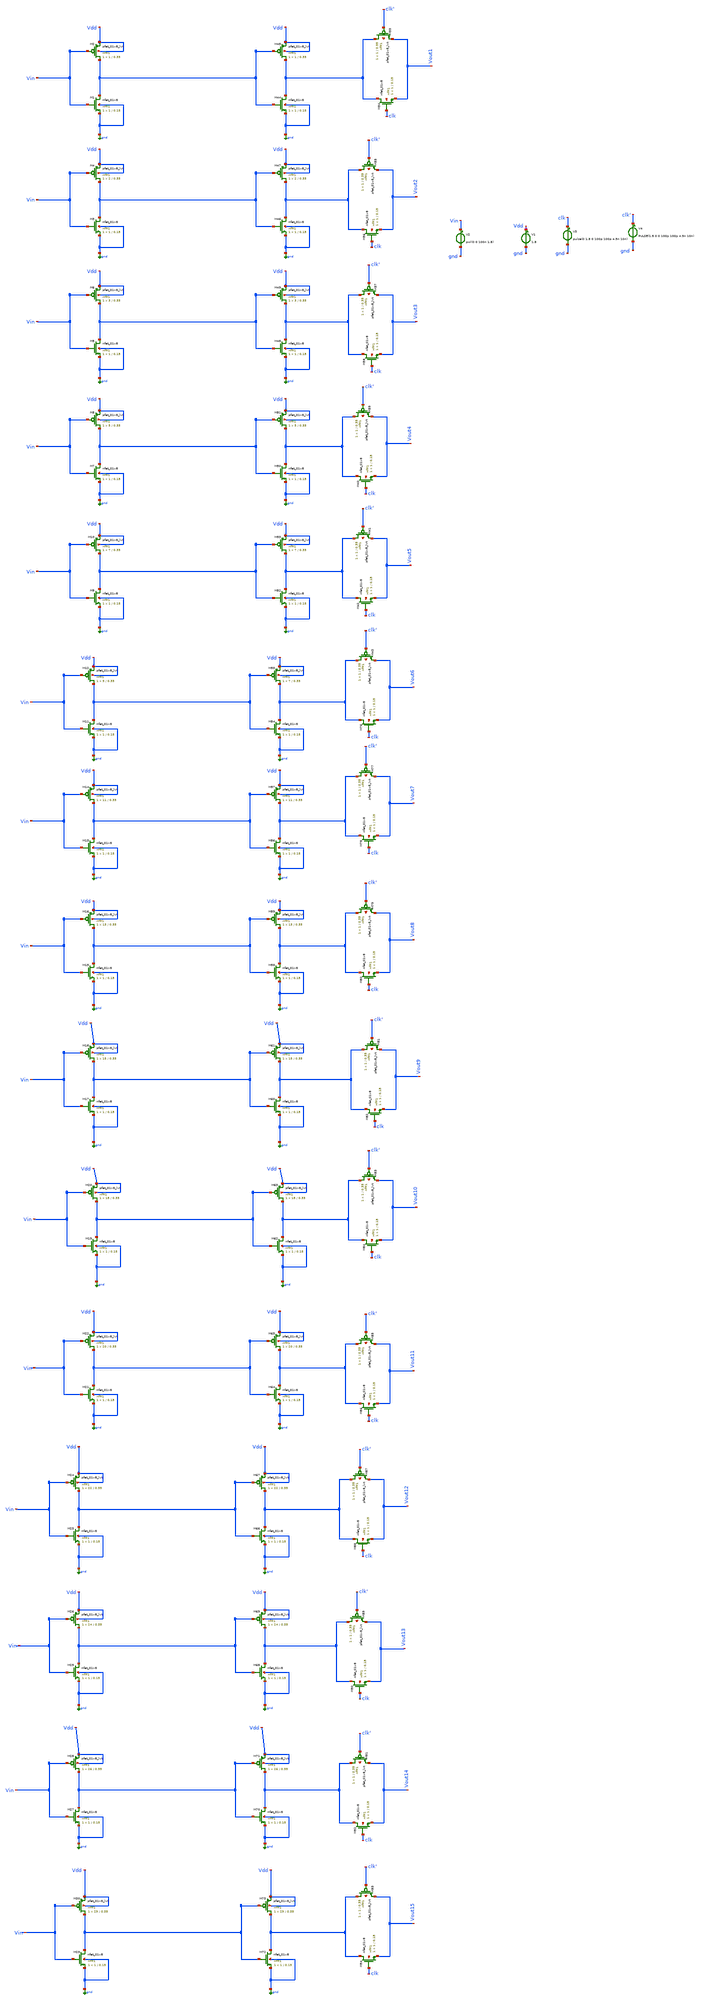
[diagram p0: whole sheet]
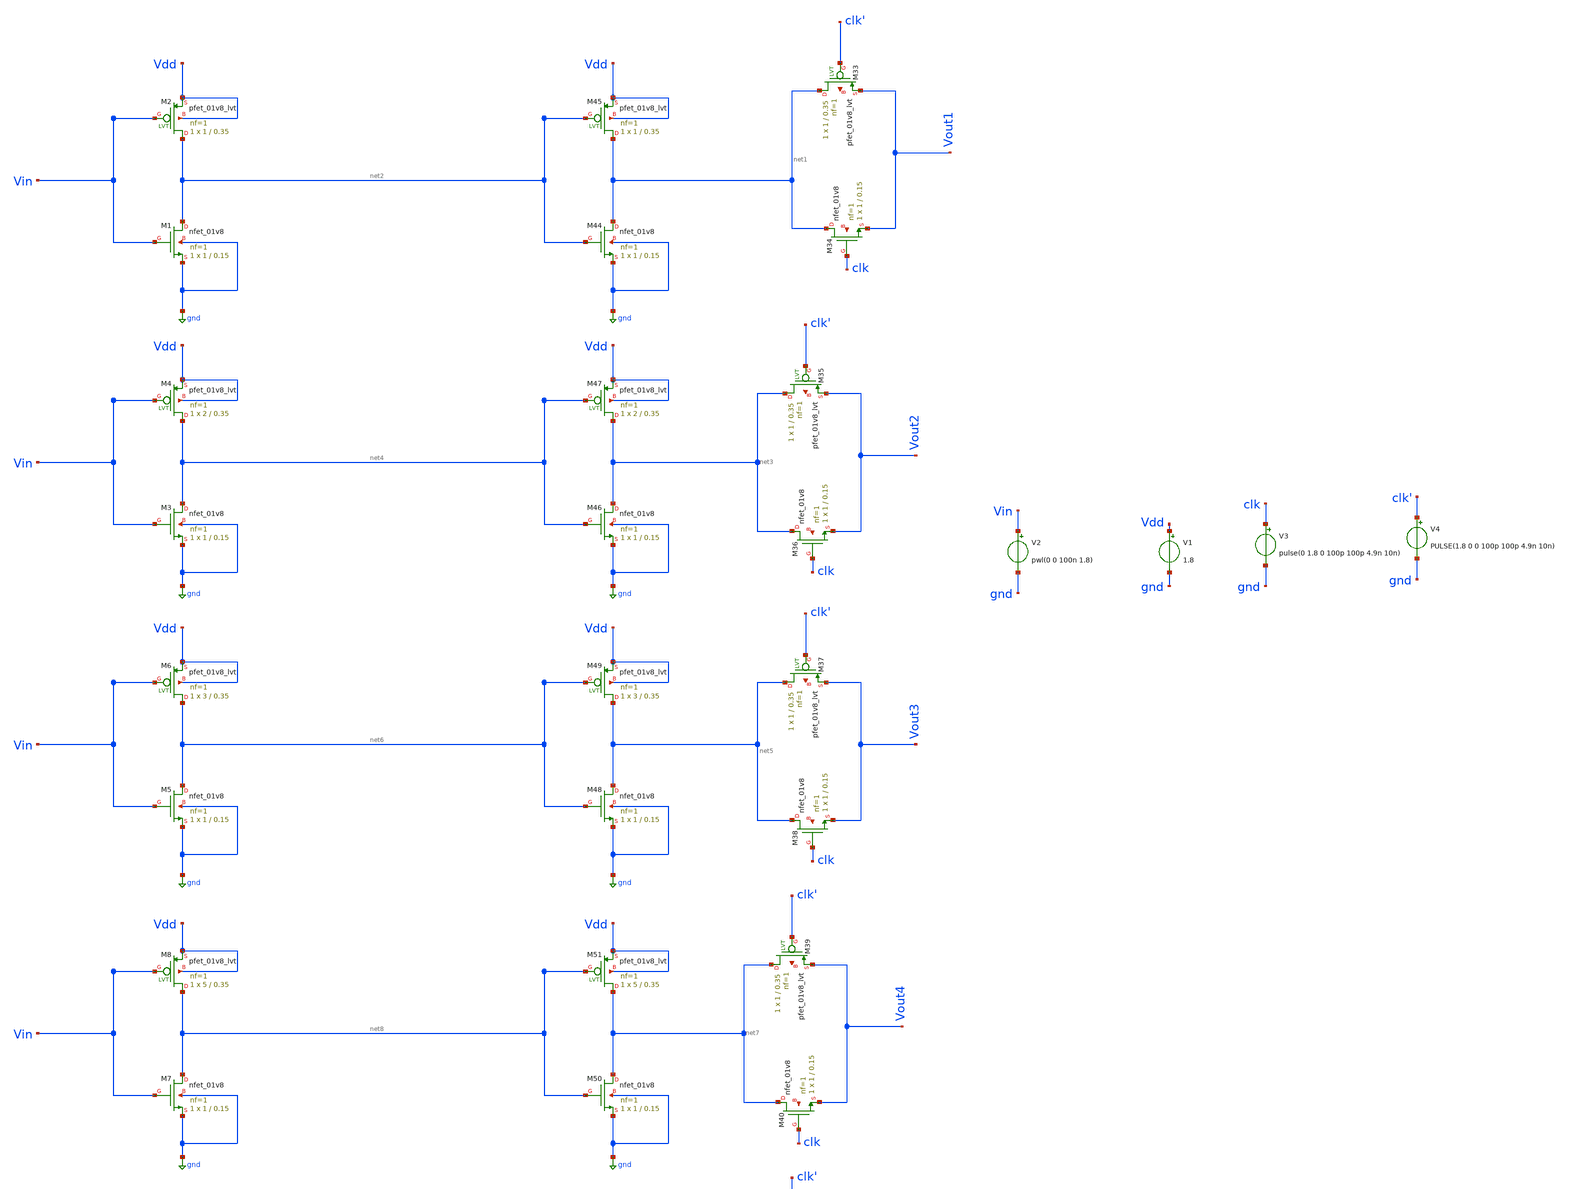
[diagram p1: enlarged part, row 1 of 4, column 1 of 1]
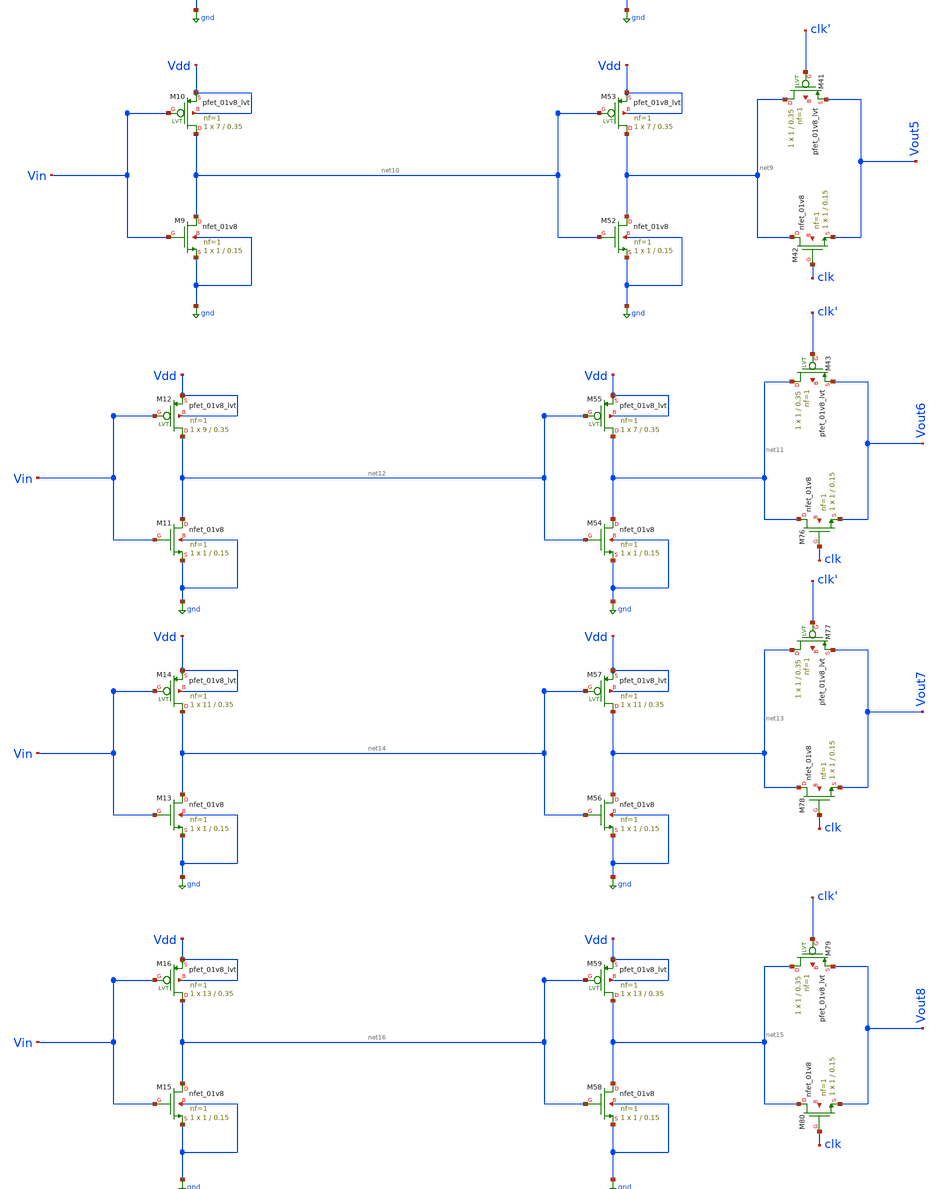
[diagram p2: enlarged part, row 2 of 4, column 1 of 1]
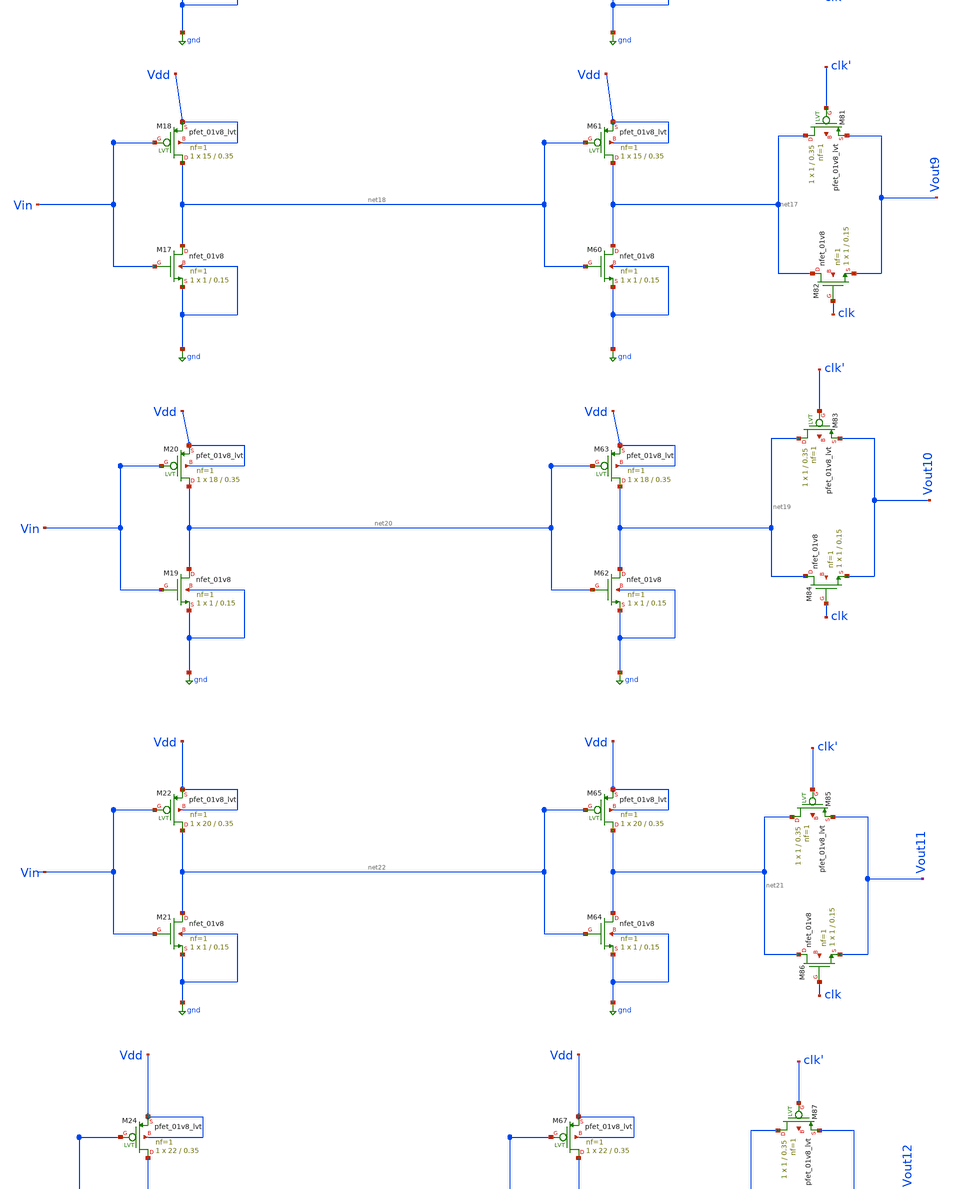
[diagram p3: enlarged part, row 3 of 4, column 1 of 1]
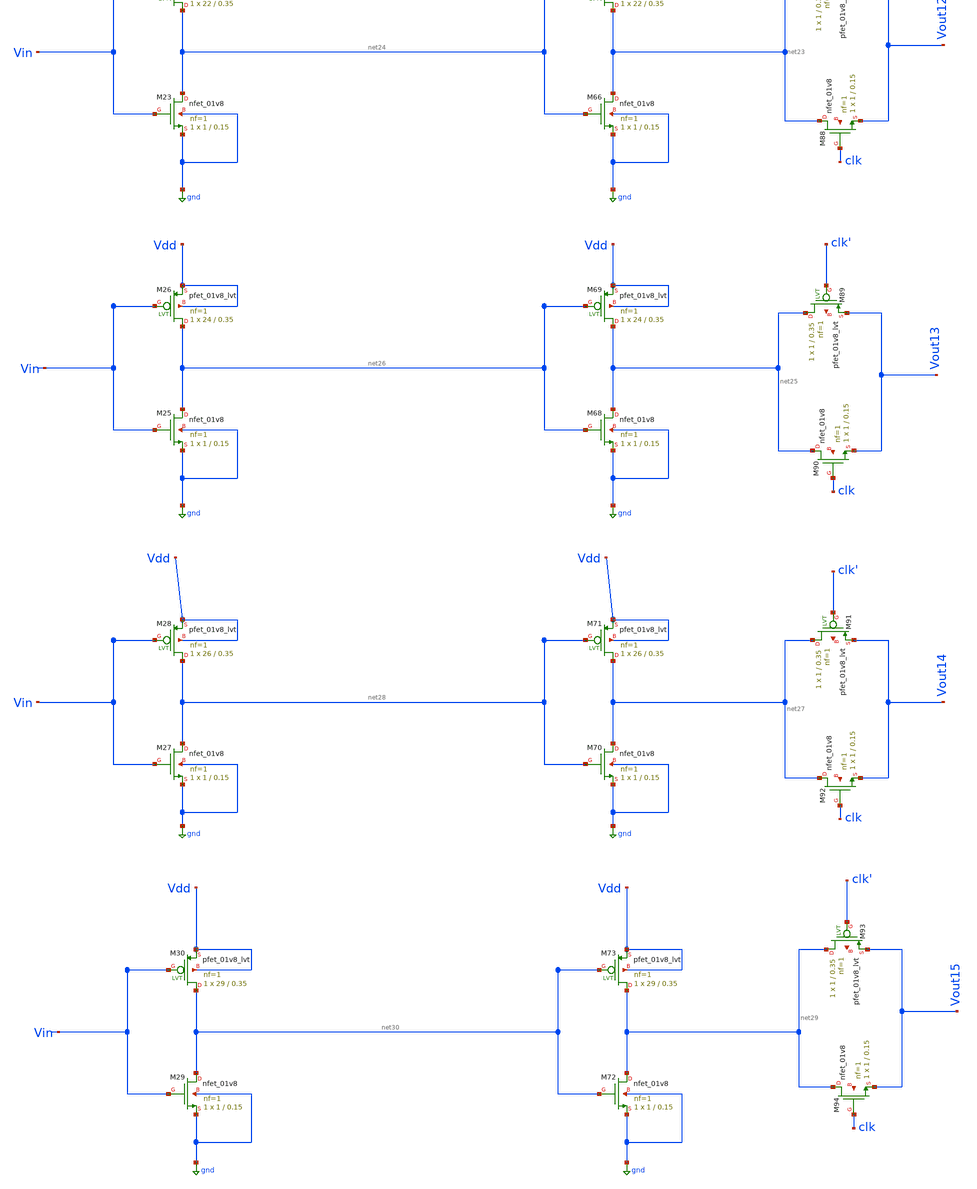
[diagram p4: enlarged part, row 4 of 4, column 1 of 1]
** sch_path: 4bit-tiq.sch
**.subckt 4bit-tiq
XM44 net1 net2 gnd gnd sky130_fd_pr__nfet_01v8 L=0.15 W=1 nf=1 ad='int((1 + 1)/2) * 1 / 1 * 0.29' as='int((1 + 2)/2) * 1 / 1 * 0.29'
+ pd='2*int((1 + 1)/2) * (1 / 1 + 0.29)' ps='2*int((1 + 2)/2) * (1 / 1 + 0.29)' nrd='0.29 / 1 ' nrs='0.29 / 1 '
+ sa=0 sb=0 sd=0 mult=1 m=1
XM45 net1 net2 Vdd Vdd sky130_fd_pr__pfet_01v8_lvt L=0.35 W=1 nf=1 ad='int((1 + 1)/2) * 1 / 1 * 0.29'
+ as='int((1 + 2)/2) * 1 / 1 * 0.29' pd='2*int((1 + 1)/2) * (1 / 1 + 0.29)' ps='2*int((1 + 2)/2) * (1 / 1 + 0.29)'
+ nrd='0.29 / 1 ' nrs='0.29 / 1 ' sa=0 sb=0 sd=0 mult=1 m=1
V1 Vdd gnd 1.8
V2 Vin gnd pwl(0 0 100n 1.8)
XM46 net3 net4 gnd gnd sky130_fd_pr__nfet_01v8 L=0.15 W=1 nf=1 ad='int((1 + 1)/2) * 1 / 1 * 0.29' as='int((1 + 2)/2) * 1 / 1 * 0.29'
+ pd='2*int((1 + 1)/2) * (1 / 1 + 0.29)' ps='2*int((1 + 2)/2) * (1 / 1 + 0.29)' nrd='0.29 / 1 ' nrs='0.29 / 1 '
+ sa=0 sb=0 sd=0 mult=1 m=1
XM47 net3 net4 Vdd Vdd sky130_fd_pr__pfet_01v8_lvt L=0.35 W=2 nf=1 ad='int((1 + 1)/2) * 2 / 1 * 0.29'
+ as='int((1 + 2)/2) * 2 / 1 * 0.29' pd='2*int((1 + 1)/2) * (2 / 1 + 0.29)' ps='2*int((1 + 2)/2) * (2 / 1 + 0.29)'
+ nrd='0.29 / 2 ' nrs='0.29 / 2 ' sa=0 sb=0 sd=0 mult=1 m=1
XM48 net5 net6 gnd gnd sky130_fd_pr__nfet_01v8 L=0.15 W=1 nf=1 ad='int((1 + 1)/2) * 1 / 1 * 0.29' as='int((1 + 2)/2) * 1 / 1 * 0.29'
+ pd='2*int((1 + 1)/2) * (1 / 1 + 0.29)' ps='2*int((1 + 2)/2) * (1 / 1 + 0.29)' nrd='0.29 / 1 ' nrs='0.29 / 1 '
+ sa=0 sb=0 sd=0 mult=1 m=1
XM49 net5 net6 Vdd Vdd sky130_fd_pr__pfet_01v8_lvt L=0.35 W=3 nf=1 ad='int((1 + 1)/2) * 3 / 1 * 0.29'
+ as='int((1 + 2)/2) * 3 / 1 * 0.29' pd='2*int((1 + 1)/2) * (3 / 1 + 0.29)' ps='2*int((1 + 2)/2) * (3 / 1 + 0.29)'
+ nrd='0.29 / 3 ' nrs='0.29 / 3 ' sa=0 sb=0 sd=0 mult=1 m=1
XM50 net7 net8 gnd gnd sky130_fd_pr__nfet_01v8 L=0.15 W=1 nf=1 ad='int((1 + 1)/2) * 1 / 1 * 0.29' as='int((1 + 2)/2) * 1 / 1 * 0.29'
+ pd='2*int((1 + 1)/2) * (1 / 1 + 0.29)' ps='2*int((1 + 2)/2) * (1 / 1 + 0.29)' nrd='0.29 / 1 ' nrs='0.29 / 1 '
+ sa=0 sb=0 sd=0 mult=1 m=1
XM51 net7 net8 Vdd Vdd sky130_fd_pr__pfet_01v8_lvt L=0.35 W=5 nf=1 ad='int((1 + 1)/2) * 5 / 1 * 0.29'
+ as='int((1 + 2)/2) * 5 / 1 * 0.29' pd='2*int((1 + 1)/2) * (5 / 1 + 0.29)' ps='2*int((1 + 2)/2) * (5 / 1 + 0.29)'
+ nrd='0.29 / 5 ' nrs='0.29 / 5 ' sa=0 sb=0 sd=0 mult=1 m=1
XM52 net9 net10 gnd gnd sky130_fd_pr__nfet_01v8 L=0.15 W=1 nf=1 ad='int((1 + 1)/2) * 1 / 1 * 0.29' as='int((1 + 2)/2) * 1 / 1 * 0.29'
+ pd='2*int((1 + 1)/2) * (1 / 1 + 0.29)' ps='2*int((1 + 2)/2) * (1 / 1 + 0.29)' nrd='0.29 / 1 ' nrs='0.29 / 1 '
+ sa=0 sb=0 sd=0 mult=1 m=1
XM53 net9 net10 Vdd Vdd sky130_fd_pr__pfet_01v8_lvt L=0.35 W=7 nf=1 ad='int((1 + 1)/2) * 7 / 1 * 0.29'
+ as='int((1 + 2)/2) * 7 / 1 * 0.29' pd='2*int((1 + 1)/2) * (7 / 1 + 0.29)' ps='2*int((1 + 2)/2) * (7 / 1 + 0.29)'
+ nrd='0.29 / 7 ' nrs='0.29 / 7 ' sa=0 sb=0 sd=0 mult=1 m=1
XM54 net11 net12 gnd gnd sky130_fd_pr__nfet_01v8 L=0.15 W=1 nf=1 ad='int((1 + 1)/2) * 1 / 1 * 0.29' as='int((1 + 2)/2) * 1 / 1 * 0.29'
+ pd='2*int((1 + 1)/2) * (1 / 1 + 0.29)' ps='2*int((1 + 2)/2) * (1 / 1 + 0.29)' nrd='0.29 / 1 ' nrs='0.29 / 1 '
+ sa=0 sb=0 sd=0 mult=1 m=1
XM55 net11 net12 Vdd Vdd sky130_fd_pr__pfet_01v8_lvt L=0.35 W=7 nf=1 ad='int((1 + 1)/2) * 7 / 1 * 0.29'
+ as='int((1 + 2)/2) * 7 / 1 * 0.29' pd='2*int((1 + 1)/2) * (7 / 1 + 0.29)' ps='2*int((1 + 2)/2) * (7 / 1 + 0.29)'
+ nrd='0.29 / 7 ' nrs='0.29 / 7 ' sa=0 sb=0 sd=0 mult=1 m=1
XM56 net13 net14 gnd gnd sky130_fd_pr__nfet_01v8 L=0.15 W=1 nf=1 ad='int((1 + 1)/2) * 1 / 1 * 0.29' as='int((1 + 2)/2) * 1 / 1 * 0.29'
+ pd='2*int((1 + 1)/2) * (1 / 1 + 0.29)' ps='2*int((1 + 2)/2) * (1 / 1 + 0.29)' nrd='0.29 / 1 ' nrs='0.29 / 1 '
+ sa=0 sb=0 sd=0 mult=1 m=1
XM57 net13 net14 Vdd Vdd sky130_fd_pr__pfet_01v8_lvt L=0.35 W=11 nf=1 ad='int((1 + 1)/2) * 11 / 1 * 0.29'
+ as='int((1 + 2)/2) * 11 / 1 * 0.29' pd='2*int((1 + 1)/2) * (11 / 1 + 0.29)' ps='2*int((1 + 2)/2) * (11 / 1 + 0.29)'
+ nrd='0.29 / 11 ' nrs='0.29 / 11 ' sa=0 sb=0 sd=0 mult=1 m=1
XM58 net15 net16 gnd gnd sky130_fd_pr__nfet_01v8 L=0.15 W=1 nf=1 ad='int((1 + 1)/2) * 1 / 1 * 0.29' as='int((1 + 2)/2) * 1 / 1 * 0.29'
+ pd='2*int((1 + 1)/2) * (1 / 1 + 0.29)' ps='2*int((1 + 2)/2) * (1 / 1 + 0.29)' nrd='0.29 / 1 ' nrs='0.29 / 1 '
+ sa=0 sb=0 sd=0 mult=1 m=1
XM59 net15 net16 Vdd Vdd sky130_fd_pr__pfet_01v8_lvt L=0.35 W=13 nf=1 ad='int((1 + 1)/2) * 13 / 1 * 0.29'
+ as='int((1 + 2)/2) * 13 / 1 * 0.29' pd='2*int((1 + 1)/2) * (13 / 1 + 0.29)' ps='2*int((1 + 2)/2) * (13 / 1 + 0.29)'
+ nrd='0.29 / 13 ' nrs='0.29 / 13 ' sa=0 sb=0 sd=0 mult=1 m=1
XM60 net17 net18 gnd gnd sky130_fd_pr__nfet_01v8 L=0.15 W=1 nf=1 ad='int((1 + 1)/2) * 1 / 1 * 0.29' as='int((1 + 2)/2) * 1 / 1 * 0.29'
+ pd='2*int((1 + 1)/2) * (1 / 1 + 0.29)' ps='2*int((1 + 2)/2) * (1 / 1 + 0.29)' nrd='0.29 / 1 ' nrs='0.29 / 1 '
+ sa=0 sb=0 sd=0 mult=1 m=1
XM61 net17 net18 Vdd Vdd sky130_fd_pr__pfet_01v8_lvt L=0.35 W=15 nf=1 ad='int((1 + 1)/2) * 15 / 1 * 0.29'
+ as='int((1 + 2)/2) * 15 / 1 * 0.29' pd='2*int((1 + 1)/2) * (15 / 1 + 0.29)' ps='2*int((1 + 2)/2) * (15 / 1 + 0.29)'
+ nrd='0.29 / 15 ' nrs='0.29 / 15 ' sa=0 sb=0 sd=0 mult=1 m=1
XM62 net19 net20 gnd gnd sky130_fd_pr__nfet_01v8 L=0.15 W=1 nf=1 ad='int((1 + 1)/2) * 1 / 1 * 0.29' as='int((1 + 2)/2) * 1 / 1 * 0.29'
+ pd='2*int((1 + 1)/2) * (1 / 1 + 0.29)' ps='2*int((1 + 2)/2) * (1 / 1 + 0.29)' nrd='0.29 / 1 ' nrs='0.29 / 1 '
+ sa=0 sb=0 sd=0 mult=1 m=1
XM63 net19 net20 Vdd Vdd sky130_fd_pr__pfet_01v8_lvt L=0.35 W=18 nf=1 ad='int((1 + 1)/2) * 18 / 1 * 0.29'
+ as='int((1 + 2)/2) * 18 / 1 * 0.29' pd='2*int((1 + 1)/2) * (18 / 1 + 0.29)' ps='2*int((1 + 2)/2) * (18 / 1 + 0.29)'
+ nrd='0.29 / 18 ' nrs='0.29 / 18 ' sa=0 sb=0 sd=0 mult=1 m=1
XM64 net21 net22 gnd gnd sky130_fd_pr__nfet_01v8 L=0.15 W=1 nf=1 ad='int((1 + 1)/2) * 1 / 1 * 0.29' as='int((1 + 2)/2) * 1 / 1 * 0.29'
+ pd='2*int((1 + 1)/2) * (1 / 1 + 0.29)' ps='2*int((1 + 2)/2) * (1 / 1 + 0.29)' nrd='0.29 / 1 ' nrs='0.29 / 1 '
+ sa=0 sb=0 sd=0 mult=1 m=1
XM65 net21 net22 Vdd Vdd sky130_fd_pr__pfet_01v8_lvt L=0.35 W=20 nf=1 ad='int((1 + 1)/2) * 20 / 1 * 0.29'
+ as='int((1 + 2)/2) * 20 / 1 * 0.29' pd='2*int((1 + 1)/2) * (20 / 1 + 0.29)' ps='2*int((1 + 2)/2) * (20 / 1 + 0.29)'
+ nrd='0.29 / 20 ' nrs='0.29 / 20 ' sa=0 sb=0 sd=0 mult=1 m=1
XM66 net23 net24 gnd gnd sky130_fd_pr__nfet_01v8 L=0.15 W=1 nf=1 ad='int((1 + 1)/2) * 1 / 1 * 0.29' as='int((1 + 2)/2) * 1 / 1 * 0.29'
+ pd='2*int((1 + 1)/2) * (1 / 1 + 0.29)' ps='2*int((1 + 2)/2) * (1 / 1 + 0.29)' nrd='0.29 / 1 ' nrs='0.29 / 1 '
+ sa=0 sb=0 sd=0 mult=1 m=1
XM67 net23 net24 Vdd Vdd sky130_fd_pr__pfet_01v8_lvt L=0.35 W=22 nf=1 ad='int((1 + 1)/2) * 22 / 1 * 0.29'
+ as='int((1 + 2)/2) * 22 / 1 * 0.29' pd='2*int((1 + 1)/2) * (22 / 1 + 0.29)' ps='2*int((1 + 2)/2) * (22 / 1 + 0.29)'
+ nrd='0.29 / 22 ' nrs='0.29 / 22 ' sa=0 sb=0 sd=0 mult=1 m=1
XM68 net25 net26 gnd gnd sky130_fd_pr__nfet_01v8 L=0.15 W=1 nf=1 ad='int((1 + 1)/2) * 1 / 1 * 0.29' as='int((1 + 2)/2) * 1 / 1 * 0.29'
+ pd='2*int((1 + 1)/2) * (1 / 1 + 0.29)' ps='2*int((1 + 2)/2) * (1 / 1 + 0.29)' nrd='0.29 / 1 ' nrs='0.29 / 1 '
+ sa=0 sb=0 sd=0 mult=1 m=1
XM69 net25 net26 Vdd Vdd sky130_fd_pr__pfet_01v8_lvt L=0.35 W=24 nf=1 ad='int((1 + 1)/2) * 24 / 1 * 0.29'
+ as='int((1 + 2)/2) * 24 / 1 * 0.29' pd='2*int((1 + 1)/2) * (24 / 1 + 0.29)' ps='2*int((1 + 2)/2) * (24 / 1 + 0.29)'
+ nrd='0.29 / 24 ' nrs='0.29 / 24 ' sa=0 sb=0 sd=0 mult=1 m=1
XM70 net27 net28 gnd gnd sky130_fd_pr__nfet_01v8 L=0.15 W=1 nf=1 ad='int((1 + 1)/2) * 1 / 1 * 0.29' as='int((1 + 2)/2) * 1 / 1 * 0.29'
+ pd='2*int((1 + 1)/2) * (1 / 1 + 0.29)' ps='2*int((1 + 2)/2) * (1 / 1 + 0.29)' nrd='0.29 / 1 ' nrs='0.29 / 1 '
+ sa=0 sb=0 sd=0 mult=1 m=1
XM71 net27 net28 Vdd Vdd sky130_fd_pr__pfet_01v8_lvt L=0.35 W=26 nf=1 ad='int((1 + 1)/2) * 26 / 1 * 0.29'
+ as='int((1 + 2)/2) * 26 / 1 * 0.29' pd='2*int((1 + 1)/2) * (26 / 1 + 0.29)' ps='2*int((1 + 2)/2) * (26 / 1 + 0.29)'
+ nrd='0.29 / 26 ' nrs='0.29 / 26 ' sa=0 sb=0 sd=0 mult=1 m=1
XM72 net29 net30 gnd gnd sky130_fd_pr__nfet_01v8 L=0.15 W=1 nf=1 ad='int((1 + 1)/2) * 1 / 1 * 0.29' as='int((1 + 2)/2) * 1 / 1 * 0.29'
+ pd='2*int((1 + 1)/2) * (1 / 1 + 0.29)' ps='2*int((1 + 2)/2) * (1 / 1 + 0.29)' nrd='0.29 / 1 ' nrs='0.29 / 1 '
+ sa=0 sb=0 sd=0 mult=1 m=1
XM73 net29 net30 Vdd Vdd sky130_fd_pr__pfet_01v8_lvt L=0.35 W=29 nf=1 ad='int((1 + 1)/2) * 29 / 1 * 0.29'
+ as='int((1 + 2)/2) * 29 / 1 * 0.29' pd='2*int((1 + 1)/2) * (29 / 1 + 0.29)' ps='2*int((1 + 2)/2) * (29 / 1 + 0.29)'
+ nrd='0.29 / 29 ' nrs='0.29 / 29 ' sa=0 sb=0 sd=0 mult=1 m=1
XM1 net2 Vin gnd gnd sky130_fd_pr__nfet_01v8 L=0.15 W=1 nf=1 ad='int((1 + 1)/2) * 1 / 1 * 0.29' as='int((1 + 2)/2) * 1 / 1 * 0.29'
+ pd='2*int((1 + 1)/2) * (1 / 1 + 0.29)' ps='2*int((1 + 2)/2) * (1 / 1 + 0.29)' nrd='0.29 / 1 ' nrs='0.29 / 1 '
+ sa=0 sb=0 sd=0 mult=1 m=1
XM2 net2 Vin Vdd Vdd sky130_fd_pr__pfet_01v8_lvt L=0.35 W=1 nf=1 ad='int((1 + 1)/2) * 1 / 1 * 0.29' as='int((1 + 2)/2) * 1 / 1 * 0.29'
+ pd='2*int((1 + 1)/2) * (1 / 1 + 0.29)' ps='2*int((1 + 2)/2) * (1 / 1 + 0.29)' nrd='0.29 / 1 ' nrs='0.29 / 1 '
+ sa=0 sb=0 sd=0 mult=1 m=1
XM3 net4 Vin gnd gnd sky130_fd_pr__nfet_01v8 L=0.15 W=1 nf=1 ad='int((1 + 1)/2) * 1 / 1 * 0.29' as='int((1 + 2)/2) * 1 / 1 * 0.29'
+ pd='2*int((1 + 1)/2) * (1 / 1 + 0.29)' ps='2*int((1 + 2)/2) * (1 / 1 + 0.29)' nrd='0.29 / 1 ' nrs='0.29 / 1 '
+ sa=0 sb=0 sd=0 mult=1 m=1
XM4 net4 Vin Vdd Vdd sky130_fd_pr__pfet_01v8_lvt L=0.35 W=2 nf=1 ad='int((1 + 1)/2) * 2 / 1 * 0.29' as='int((1 + 2)/2) * 2 / 1 * 0.29'
+ pd='2*int((1 + 1)/2) * (2 / 1 + 0.29)' ps='2*int((1 + 2)/2) * (2 / 1 + 0.29)' nrd='0.29 / 2 ' nrs='0.29 / 2 '
+ sa=0 sb=0 sd=0 mult=1 m=1
XM5 net6 Vin gnd gnd sky130_fd_pr__nfet_01v8 L=0.15 W=1 nf=1 ad='int((1 + 1)/2) * 1 / 1 * 0.29' as='int((1 + 2)/2) * 1 / 1 * 0.29'
+ pd='2*int((1 + 1)/2) * (1 / 1 + 0.29)' ps='2*int((1 + 2)/2) * (1 / 1 + 0.29)' nrd='0.29 / 1 ' nrs='0.29 / 1 '
+ sa=0 sb=0 sd=0 mult=1 m=1
XM6 net6 Vin Vdd Vdd sky130_fd_pr__pfet_01v8_lvt L=0.35 W=3 nf=1 ad='int((1 + 1)/2) * 3 / 1 * 0.29' as='int((1 + 2)/2) * 3 / 1 * 0.29'
+ pd='2*int((1 + 1)/2) * (3 / 1 + 0.29)' ps='2*int((1 + 2)/2) * (3 / 1 + 0.29)' nrd='0.29 / 3 ' nrs='0.29 / 3 '
+ sa=0 sb=0 sd=0 mult=1 m=1
XM7 net8 Vin gnd gnd sky130_fd_pr__nfet_01v8 L=0.15 W=1 nf=1 ad='int((1 + 1)/2) * 1 / 1 * 0.29' as='int((1 + 2)/2) * 1 / 1 * 0.29'
+ pd='2*int((1 + 1)/2) * (1 / 1 + 0.29)' ps='2*int((1 + 2)/2) * (1 / 1 + 0.29)' nrd='0.29 / 1 ' nrs='0.29 / 1 '
+ sa=0 sb=0 sd=0 mult=1 m=1
XM8 net8 Vin Vdd Vdd sky130_fd_pr__pfet_01v8_lvt L=0.35 W=5 nf=1 ad='int((1 + 1)/2) * 5 / 1 * 0.29' as='int((1 + 2)/2) * 5 / 1 * 0.29'
+ pd='2*int((1 + 1)/2) * (5 / 1 + 0.29)' ps='2*int((1 + 2)/2) * (5 / 1 + 0.29)' nrd='0.29 / 5 ' nrs='0.29 / 5 '
+ sa=0 sb=0 sd=0 mult=1 m=1
XM9 net10 Vin gnd gnd sky130_fd_pr__nfet_01v8 L=0.15 W=1 nf=1 ad='int((1 + 1)/2) * 1 / 1 * 0.29' as='int((1 + 2)/2) * 1 / 1 * 0.29'
+ pd='2*int((1 + 1)/2) * (1 / 1 + 0.29)' ps='2*int((1 + 2)/2) * (1 / 1 + 0.29)' nrd='0.29 / 1 ' nrs='0.29 / 1 '
+ sa=0 sb=0 sd=0 mult=1 m=1
XM10 net10 Vin Vdd Vdd sky130_fd_pr__pfet_01v8_lvt L=0.35 W=7 nf=1 ad='int((1 + 1)/2) * 7 / 1 * 0.29'
+ as='int((1 + 2)/2) * 7 / 1 * 0.29' pd='2*int((1 + 1)/2) * (7 / 1 + 0.29)' ps='2*int((1 + 2)/2) * (7 / 1 + 0.29)'
+ nrd='0.29 / 7 ' nrs='0.29 / 7 ' sa=0 sb=0 sd=0 mult=1 m=1
XM11 net12 Vin gnd gnd sky130_fd_pr__nfet_01v8 L=0.15 W=1 nf=1 ad='int((1 + 1)/2) * 1 / 1 * 0.29' as='int((1 + 2)/2) * 1 / 1 * 0.29'
+ pd='2*int((1 + 1)/2) * (1 / 1 + 0.29)' ps='2*int((1 + 2)/2) * (1 / 1 + 0.29)' nrd='0.29 / 1 ' nrs='0.29 / 1 '
+ sa=0 sb=0 sd=0 mult=1 m=1
XM12 net12 Vin Vdd Vdd sky130_fd_pr__pfet_01v8_lvt L=0.35 W=9 nf=1 ad='int((1 + 1)/2) * 9 / 1 * 0.29'
+ as='int((1 + 2)/2) * 9 / 1 * 0.29' pd='2*int((1 + 1)/2) * (9 / 1 + 0.29)' ps='2*int((1 + 2)/2) * (9 / 1 + 0.29)'
+ nrd='0.29 / 9 ' nrs='0.29 / 9 ' sa=0 sb=0 sd=0 mult=1 m=1
XM13 net14 Vin gnd gnd sky130_fd_pr__nfet_01v8 L=0.15 W=1 nf=1 ad='int((1 + 1)/2) * 1 / 1 * 0.29' as='int((1 + 2)/2) * 1 / 1 * 0.29'
+ pd='2*int((1 + 1)/2) * (1 / 1 + 0.29)' ps='2*int((1 + 2)/2) * (1 / 1 + 0.29)' nrd='0.29 / 1 ' nrs='0.29 / 1 '
+ sa=0 sb=0 sd=0 mult=1 m=1
XM14 net14 Vin Vdd Vdd sky130_fd_pr__pfet_01v8_lvt L=0.35 W=11 nf=1 ad='int((1 + 1)/2) * 11 / 1 * 0.29'
+ as='int((1 + 2)/2) * 11 / 1 * 0.29' pd='2*int((1 + 1)/2) * (11 / 1 + 0.29)' ps='2*int((1 + 2)/2) * (11 / 1 + 0.29)'
+ nrd='0.29 / 11 ' nrs='0.29 / 11 ' sa=0 sb=0 sd=0 mult=1 m=1
XM15 net16 Vin gnd gnd sky130_fd_pr__nfet_01v8 L=0.15 W=1 nf=1 ad='int((1 + 1)/2) * 1 / 1 * 0.29' as='int((1 + 2)/2) * 1 / 1 * 0.29'
+ pd='2*int((1 + 1)/2) * (1 / 1 + 0.29)' ps='2*int((1 + 2)/2) * (1 / 1 + 0.29)' nrd='0.29 / 1 ' nrs='0.29 / 1 '
+ sa=0 sb=0 sd=0 mult=1 m=1
XM16 net16 Vin Vdd Vdd sky130_fd_pr__pfet_01v8_lvt L=0.35 W=13 nf=1 ad='int((1 + 1)/2) * 13 / 1 * 0.29'
+ as='int((1 + 2)/2) * 13 / 1 * 0.29' pd='2*int((1 + 1)/2) * (13 / 1 + 0.29)' ps='2*int((1 + 2)/2) * (13 / 1 + 0.29)'
+ nrd='0.29 / 13 ' nrs='0.29 / 13 ' sa=0 sb=0 sd=0 mult=1 m=1
XM17 net18 Vin gnd gnd sky130_fd_pr__nfet_01v8 L=0.15 W=1 nf=1 ad='int((1 + 1)/2) * 1 / 1 * 0.29' as='int((1 + 2)/2) * 1 / 1 * 0.29'
+ pd='2*int((1 + 1)/2) * (1 / 1 + 0.29)' ps='2*int((1 + 2)/2) * (1 / 1 + 0.29)' nrd='0.29 / 1 ' nrs='0.29 / 1 '
+ sa=0 sb=0 sd=0 mult=1 m=1
XM18 net18 Vin Vdd Vdd sky130_fd_pr__pfet_01v8_lvt L=0.35 W=15 nf=1 ad='int((1 + 1)/2) * 15 / 1 * 0.29'
+ as='int((1 + 2)/2) * 15 / 1 * 0.29' pd='2*int((1 + 1)/2) * (15 / 1 + 0.29)' ps='2*int((1 + 2)/2) * (15 / 1 + 0.29)'
+ nrd='0.29 / 15 ' nrs='0.29 / 15 ' sa=0 sb=0 sd=0 mult=1 m=1
XM19 net20 Vin gnd gnd sky130_fd_pr__nfet_01v8 L=0.15 W=1 nf=1 ad='int((1 + 1)/2) * 1 / 1 * 0.29' as='int((1 + 2)/2) * 1 / 1 * 0.29'
+ pd='2*int((1 + 1)/2) * (1 / 1 + 0.29)' ps='2*int((1 + 2)/2) * (1 / 1 + 0.29)' nrd='0.29 / 1 ' nrs='0.29 / 1 '
+ sa=0 sb=0 sd=0 mult=1 m=1
XM20 net20 Vin Vdd Vdd sky130_fd_pr__pfet_01v8_lvt L=0.35 W=18 nf=1 ad='int((1 + 1)/2) * 18 / 1 * 0.29'
+ as='int((1 + 2)/2) * 18 / 1 * 0.29' pd='2*int((1 + 1)/2) * (18 / 1 + 0.29)' ps='2*int((1 + 2)/2) * (18 / 1 + 0.29)'
+ nrd='0.29 / 18 ' nrs='0.29 / 18 ' sa=0 sb=0 sd=0 mult=1 m=1
XM21 net22 Vin gnd gnd sky130_fd_pr__nfet_01v8 L=0.15 W=1 nf=1 ad='int((1 + 1)/2) * 1 / 1 * 0.29' as='int((1 + 2)/2) * 1 / 1 * 0.29'
+ pd='2*int((1 + 1)/2) * (1 / 1 + 0.29)' ps='2*int((1 + 2)/2) * (1 / 1 + 0.29)' nrd='0.29 / 1 ' nrs='0.29 / 1 '
+ sa=0 sb=0 sd=0 mult=1 m=1
XM22 net22 Vin Vdd Vdd sky130_fd_pr__pfet_01v8_lvt L=0.35 W=20 nf=1 ad='int((1 + 1)/2) * 20 / 1 * 0.29'
+ as='int((1 + 2)/2) * 20 / 1 * 0.29' pd='2*int((1 + 1)/2) * (20 / 1 + 0.29)' ps='2*int((1 + 2)/2) * (20 / 1 + 0.29)'
+ nrd='0.29 / 20 ' nrs='0.29 / 20 ' sa=0 sb=0 sd=0 mult=1 m=1
XM23 net24 Vin gnd gnd sky130_fd_pr__nfet_01v8 L=0.15 W=1 nf=1 ad='int((1 + 1)/2) * 1 / 1 * 0.29' as='int((1 + 2)/2) * 1 / 1 * 0.29'
+ pd='2*int((1 + 1)/2) * (1 / 1 + 0.29)' ps='2*int((1 + 2)/2) * (1 / 1 + 0.29)' nrd='0.29 / 1 ' nrs='0.29 / 1 '
+ sa=0 sb=0 sd=0 mult=1 m=1
XM24 net24 Vin Vdd Vdd sky130_fd_pr__pfet_01v8_lvt L=0.35 W=22 nf=1 ad='int((1 + 1)/2) * 22 / 1 * 0.29'
+ as='int((1 + 2)/2) * 22 / 1 * 0.29' pd='2*int((1 + 1)/2) * (22 / 1 + 0.29)' ps='2*int((1 + 2)/2) * (22 / 1 + 0.29)'
+ nrd='0.29 / 22 ' nrs='0.29 / 22 ' sa=0 sb=0 sd=0 mult=1 m=1
XM25 net26 Vin gnd gnd sky130_fd_pr__nfet_01v8 L=0.15 W=1 nf=1 ad='int((1 + 1)/2) * 1 / 1 * 0.29' as='int((1 + 2)/2) * 1 / 1 * 0.29'
+ pd='2*int((1 + 1)/2) * (1 / 1 + 0.29)' ps='2*int((1 + 2)/2) * (1 / 1 + 0.29)' nrd='0.29 / 1 ' nrs='0.29 / 1 '
+ sa=0 sb=0 sd=0 mult=1 m=1
XM26 net26 Vin Vdd Vdd sky130_fd_pr__pfet_01v8_lvt L=0.35 W=24 nf=1 ad='int((1 + 1)/2) * 24 / 1 * 0.29'
+ as='int((1 + 2)/2) * 24 / 1 * 0.29' pd='2*int((1 + 1)/2) * (24 / 1 + 0.29)' ps='2*int((1 + 2)/2) * (24 / 1 + 0.29)'
+ nrd='0.29 / 24 ' nrs='0.29 / 24 ' sa=0 sb=0 sd=0 mult=1 m=1
XM27 net28 Vin gnd gnd sky130_fd_pr__nfet_01v8 L=0.15 W=1 nf=1 ad='int((1 + 1)/2) * 1 / 1 * 0.29' as='int((1 + 2)/2) * 1 / 1 * 0.29'
+ pd='2*int((1 + 1)/2) * (1 / 1 + 0.29)' ps='2*int((1 + 2)/2) * (1 / 1 + 0.29)' nrd='0.29 / 1 ' nrs='0.29 / 1 '
+ sa=0 sb=0 sd=0 mult=1 m=1
XM28 net28 Vin Vdd Vdd sky130_fd_pr__pfet_01v8_lvt L=0.35 W=26 nf=1 ad='int((1 + 1)/2) * 26 / 1 * 0.29'
+ as='int((1 + 2)/2) * 26 / 1 * 0.29' pd='2*int((1 + 1)/2) * (26 / 1 + 0.29)' ps='2*int((1 + 2)/2) * (26 / 1 + 0.29)'
+ nrd='0.29 / 26 ' nrs='0.29 / 26 ' sa=0 sb=0 sd=0 mult=1 m=1
XM29 net30 Vin gnd gnd sky130_fd_pr__nfet_01v8 L=0.15 W=1 nf=1 ad='int((1 + 1)/2) * 1 / 1 * 0.29' as='int((1 + 2)/2) * 1 / 1 * 0.29'
+ pd='2*int((1 + 1)/2) * (1 / 1 + 0.29)' ps='2*int((1 + 2)/2) * (1 / 1 + 0.29)' nrd='0.29 / 1 ' nrs='0.29 / 1 '
+ sa=0 sb=0 sd=0 mult=1 m=1
XM30 net30 Vin Vdd Vdd sky130_fd_pr__pfet_01v8_lvt L=0.35 W=29 nf=1 ad='int((1 + 1)/2) * 29 / 1 * 0.29'
+ as='int((1 + 2)/2) * 29 / 1 * 0.29' pd='2*int((1 + 1)/2) * (29 / 1 + 0.29)' ps='2*int((1 + 2)/2) * (29 / 1 + 0.29)'
+ nrd='0.29 / 29 ' nrs='0.29 / 29 ' sa=0 sb=0 sd=0 mult=1 m=1
XM33 net1 clk' Vout1 net31 sky130_fd_pr__pfet_01v8_lvt L=0.35 W=1 nf=1 ad='int((1 + 1)/2) * 1 / 1 * 0.29' as='int((1
+ + 2)/2) * 1 / 1 * 0.29' pd='2*int((1 + 1)/2) * (1 / 1 + 0.29)' ps='2*int((1 + 2)/2) * (1 / 1 + 0.29)' nrd='0.29
+ / 1 ' nrs='0.29 / 1 ' sa=0 sb=0 sd=0 mult=1 m=1
XM34 net1 clk Vout1 net32 sky130_fd_pr__nfet_01v8 L=0.15 W=1 nf=1 ad='int((1 + 1)/2) * 1 / 1 * 0.29' as='int((1
+ + 2)/2) * 1 / 1 * 0.29' pd='2*int((1 + 1)/2) * (1 / 1 + 0.29)' ps='2*int((1 + 2)/2) * (1 / 1 + 0.29)' nrd='0.29
+ / 1 ' nrs='0.29 / 1 ' sa=0 sb=0 sd=0 mult=1 m=1
XM35 net3 clk' Vout2 net33 sky130_fd_pr__pfet_01v8_lvt L=0.35 W=1 nf=1 ad='int((1 + 1)/2) * 1 / 1 * 0.29'
+ as='int((1 + 2)/2) * 1 / 1 * 0.29' pd='2*int((1 + 1)/2) * (1 / 1 + 0.29)' ps='2*int((1 + 2)/2) * (1 / 1 + 0.29)'
+ nrd='0.29 / 1 ' nrs='0.29 / 1 ' sa=0 sb=0 sd=0 mult=1 m=1
XM36 net3 clk Vout2 net34 sky130_fd_pr__nfet_01v8 L=0.15 W=1 nf=1 ad='int((1 + 1)/2) * 1 / 1 * 0.29'
+ as='int((1 + 2)/2) * 1 / 1 * 0.29' pd='2*int((1 + 1)/2) * (1 / 1 + 0.29)' ps='2*int((1 + 2)/2) * (1 / 1 + 0.29)'
+ nrd='0.29 / 1 ' nrs='0.29 / 1 ' sa=0 sb=0 sd=0 mult=1 m=1
XM37 net5 clk' Vout3 net35 sky130_fd_pr__pfet_01v8_lvt L=0.35 W=1 nf=1 ad='int((1 + 1)/2) * 1 / 1 * 0.29' as='int((1
+ + 2)/2) * 1 / 1 * 0.29' pd='2*int((1 + 1)/2) * (1 / 1 + 0.29)' ps='2*int((1 + 2)/2) * (1 / 1 + 0.29)' nrd='0.29
+ / 1 ' nrs='0.29 / 1 ' sa=0 sb=0 sd=0 mult=1 m=1
XM38 net5 clk Vout3 net36 sky130_fd_pr__nfet_01v8 L=0.15 W=1 nf=1 ad='int((1 + 1)/2) * 1 / 1 * 0.29' as='int((1
+ + 2)/2) * 1 / 1 * 0.29' pd='2*int((1 + 1)/2) * (1 / 1 + 0.29)' ps='2*int((1 + 2)/2) * (1 / 1 + 0.29)' nrd='0.29
+ / 1 ' nrs='0.29 / 1 ' sa=0 sb=0 sd=0 mult=1 m=1
XM39 net7 clk' Vout4 net37 sky130_fd_pr__pfet_01v8_lvt L=0.35 W=1 nf=1 ad='int((1 + 1)/2) * 1 / 1 * 0.29'
+ as='int((1 + 2)/2) * 1 / 1 * 0.29' pd='2*int((1 + 1)/2) * (1 / 1 + 0.29)' ps='2*int((1 + 2)/2) * (1 / 1 + 0.29)'
+ nrd='0.29 / 1 ' nrs='0.29 / 1 ' sa=0 sb=0 sd=0 mult=1 m=1
XM40 net7 clk Vout4 net38 sky130_fd_pr__nfet_01v8 L=0.15 W=1 nf=1 ad='int((1 + 1)/2) * 1 / 1 * 0.29'
+ as='int((1 + 2)/2) * 1 / 1 * 0.29' pd='2*int((1 + 1)/2) * (1 / 1 + 0.29)' ps='2*int((1 + 2)/2) * (1 / 1 + 0.29)'
+ nrd='0.29 / 1 ' nrs='0.29 / 1 ' sa=0 sb=0 sd=0 mult=1 m=1
XM41 net9 clk' Vout5 net39 sky130_fd_pr__pfet_01v8_lvt L=0.35 W=1 nf=1 ad='int((1 + 1)/2) * 1 / 1 * 0.29' as='int((1
+ + 2)/2) * 1 / 1 * 0.29' pd='2*int((1 + 1)/2) * (1 / 1 + 0.29)' ps='2*int((1 + 2)/2) * (1 / 1 + 0.29)' nrd='0.29
+ / 1 ' nrs='0.29 / 1 ' sa=0 sb=0 sd=0 mult=1 m=1
XM42 net9 clk Vout5 net40 sky130_fd_pr__nfet_01v8 L=0.15 W=1 nf=1 ad='int((1 + 1)/2) * 1 / 1 * 0.29' as='int((1
+ + 2)/2) * 1 / 1 * 0.29' pd='2*int((1 + 1)/2) * (1 / 1 + 0.29)' ps='2*int((1 + 2)/2) * (1 / 1 + 0.29)' nrd='0.29
+ / 1 ' nrs='0.29 / 1 ' sa=0 sb=0 sd=0 mult=1 m=1
XM43 net11 clk' Vout6 net41 sky130_fd_pr__pfet_01v8_lvt L=0.35 W=1 nf=1 ad='int((1 + 1)/2) * 1 / 1 * 0.29'
+ as='int((1 + 2)/2) * 1 / 1 * 0.29' pd='2*int((1 + 1)/2) * (1 / 1 + 0.29)' ps='2*int((1 + 2)/2) * (1 / 1 + 0.29)'
+ nrd='0.29 / 1 ' nrs='0.29 / 1 ' sa=0 sb=0 sd=0 mult=1 m=1
XM76 net11 clk Vout6 net42 sky130_fd_pr__nfet_01v8 L=0.15 W=1 nf=1 ad='int((1 + 1)/2) * 1 / 1 * 0.29'
+ as='int((1 + 2)/2) * 1 / 1 * 0.29' pd='2*int((1 + 1)/2) * (1 / 1 + 0.29)' ps='2*int((1 + 2)/2) * (1 / 1 + 0.29)'
+ nrd='0.29 / 1 ' nrs='0.29 / 1 ' sa=0 sb=0 sd=0 mult=1 m=1
XM77 net13 clk' Vout7 net43 sky130_fd_pr__pfet_01v8_lvt L=0.35 W=1 nf=1 ad='int((1 + 1)/2) * 1 / 1 *
+ 0.29' as='int((1 + 2)/2) * 1 / 1 * 0.29' pd='2*int((1 + 1)/2) * (1 / 1 + 0.29)' ps='2*int((1 + 2)/2)
+ * (1 / 1 + 0.29)' nrd='0.29 / 1 ' nrs='0.29 / 1 ' sa=0 sb=0 sd=0 mult=1 m=1
XM78 net13 clk Vout7 net44 sky130_fd_pr__nfet_01v8 L=0.15 W=1 nf=1 ad='int((1 + 1)/2) * 1 / 1 * 0.29' as='int((1
+ + 2)/2) * 1 / 1 * 0.29' pd='2*int((1 + 1)/2) * (1 / 1 + 0.29)' ps='2*int((1 + 2)/2) * (1 / 1 + 0.29)' nrd='0.29
+ / 1 ' nrs='0.29 / 1 ' sa=0 sb=0 sd=0 mult=1 m=1
XM79 net15 clk' Vout8 net45 sky130_fd_pr__pfet_01v8_lvt L=0.35 W=1 nf=1 ad='int((1 + 1)/2) * 1 / 1 * 0.29'
+ as='int((1 + 2)/2) * 1 / 1 * 0.29' pd='2*int((1 + 1)/2) * (1 / 1 + 0.29)' ps='2*int((1 + 2)/2) * (1 / 1 + 0.29)'
+ nrd='0.29 / 1 ' nrs='0.29 / 1 ' sa=0 sb=0 sd=0 mult=1 m=1
XM80 net15 clk Vout8 net46 sky130_fd_pr__nfet_01v8 L=0.15 W=1 nf=1 ad='int((1 + 1)/2) * 1 / 1 * 0.29'
+ as='int((1 + 2)/2) * 1 / 1 * 0.29' pd='2*int((1 + 1)/2) * (1 / 1 + 0.29)' ps='2*int((1 + 2)/2) * (1 / 1 + 0.29)'
+ nrd='0.29 / 1 ' nrs='0.29 / 1 ' sa=0 sb=0 sd=0 mult=1 m=1
XM81 net17 clk' Vout9 net47 sky130_fd_pr__pfet_01v8_lvt L=0.35 W=1 nf=1 ad='int((1 + 1)/2) * 1 / 1 *
+ 0.29' as='int((1 + 2)/2) * 1 / 1 * 0.29' pd='2*int((1 + 1)/2) * (1 / 1 + 0.29)' ps='2*int((1 + 2)/2)
+ * (1 / 1 + 0.29)' nrd='0.29 / 1 ' nrs='0.29 / 1 ' sa=0 sb=0 sd=0 mult=1 m=1
XM82 net17 clk Vout9 net48 sky130_fd_pr__nfet_01v8 L=0.15 W=1 nf=1 ad='int((1 + 1)/2) * 1 / 1 * 0.29' as='int((1
+ + 2)/2) * 1 / 1 * 0.29' pd='2*int((1 + 1)/2) * (1 / 1 + 0.29)' ps='2*int((1 + 2)/2) * (1 / 1 + 0.29)' nrd='0.29
+ / 1 ' nrs='0.29 / 1 ' sa=0 sb=0 sd=0 mult=1 m=1
XM83 net19 clk' Vout10 net49 sky130_fd_pr__pfet_01v8_lvt L=0.35 W=1 nf=1 ad='int((1 + 1)/2) * 1 / 1 * 0.29'
+ as='int((1 + 2)/2) * 1 / 1 * 0.29' pd='2*int((1 + 1)/2) * (1 / 1 + 0.29)' ps='2*int((1 + 2)/2) * (1 / 1 + 0.29)'
+ nrd='0.29 / 1 ' nrs='0.29 / 1 ' sa=0 sb=0 sd=0 mult=1 m=1
XM84 net19 clk Vout10 net50 sky130_fd_pr__nfet_01v8 L=0.15 W=1 nf=1 ad='int((1 + 1)/2) * 1 / 1 * 0.29'
+ as='int((1 + 2)/2) * 1 / 1 * 0.29' pd='2*int((1 + 1)/2) * (1 / 1 + 0.29)' ps='2*int((1 + 2)/2) * (1 / 1 + 0.29)'
+ nrd='0.29 / 1 ' nrs='0.29 / 1 ' sa=0 sb=0 sd=0 mult=1 m=1
XM85 net21 clk' Vout11 net51 sky130_fd_pr__pfet_01v8_lvt L=0.35 W=1 nf=1 ad='int((1 + 1)/2) * 1 / 1 *
+ 0.29' as='int((1 + 2)/2) * 1 / 1 * 0.29' pd='2*int((1 + 1)/2) * (1 / 1 + 0.29)' ps='2*int((1 + 2)/2)
+ * (1 / 1 + 0.29)' nrd='0.29 / 1 ' nrs='0.29 / 1 ' sa=0 sb=0 sd=0 mult=1 m=1
XM86 net21 clk Vout11 net52 sky130_fd_pr__nfet_01v8 L=0.15 W=1 nf=1 ad='int((1 + 1)/2) * 1 / 1 * 0.29' as='int((1
+ + 2)/2) * 1 / 1 * 0.29' pd='2*int((1 + 1)/2) * (1 / 1 + 0.29)' ps='2*int((1 + 2)/2) * (1 / 1 + 0.29)' nrd='0.29
+ / 1 ' nrs='0.29 / 1 ' sa=0 sb=0 sd=0 mult=1 m=1
XM87 net23 clk' Vout12 net53 sky130_fd_pr__pfet_01v8_lvt L=0.35 W=1 nf=1 ad='int((1 + 1)/2) * 1 / 1 * 0.29'
+ as='int((1 + 2)/2) * 1 / 1 * 0.29' pd='2*int((1 + 1)/2) * (1 / 1 + 0.29)' ps='2*int((1 + 2)/2) * (1 / 1 + 0.29)'
+ nrd='0.29 / 1 ' nrs='0.29 / 1 ' sa=0 sb=0 sd=0 mult=1 m=1
XM88 net23 clk Vout12 net54 sky130_fd_pr__nfet_01v8 L=0.15 W=1 nf=1 ad='int((1 + 1)/2) * 1 / 1 * 0.29'
+ as='int((1 + 2)/2) * 1 / 1 * 0.29' pd='2*int((1 + 1)/2) * (1 / 1 + 0.29)' ps='2*int((1 + 2)/2) * (1 / 1 + 0.29)'
+ nrd='0.29 / 1 ' nrs='0.29 / 1 ' sa=0 sb=0 sd=0 mult=1 m=1
XM89 net25 clk' Vout13 net55 sky130_fd_pr__pfet_01v8_lvt L=0.35 W=1 nf=1 ad='int((1 + 1)/2) * 1 / 1 *
+ 0.29' as='int((1 + 2)/2) * 1 / 1 * 0.29' pd='2*int((1 + 1)/2) * (1 / 1 + 0.29)' ps='2*int((1 + 2)/2)
+ * (1 / 1 + 0.29)' nrd='0.29 / 1 ' nrs='0.29 / 1 ' sa=0 sb=0 sd=0 mult=1 m=1
XM90 net25 clk Vout13 net56 sky130_fd_pr__nfet_01v8 L=0.15 W=1 nf=1 ad='int((1 + 1)/2) * 1 / 1 * 0.29' as='int((1
+ + 2)/2) * 1 / 1 * 0.29' pd='2*int((1 + 1)/2) * (1 / 1 + 0.29)' ps='2*int((1 + 2)/2) * (1 / 1 + 0.29)' nrd='0.29
+ / 1 ' nrs='0.29 / 1 ' sa=0 sb=0 sd=0 mult=1 m=1
XM91 net27 clk' Vout14 net57 sky130_fd_pr__pfet_01v8_lvt L=0.35 W=1 nf=1 ad='int((1 + 1)/2) * 1 / 1 * 0.29'
+ as='int((1 + 2)/2) * 1 / 1 * 0.29' pd='2*int((1 + 1)/2) * (1 / 1 + 0.29)' ps='2*int((1 + 2)/2) * (1 / 1 + 0.29)'
+ nrd='0.29 / 1 ' nrs='0.29 / 1 ' sa=0 sb=0 sd=0 mult=1 m=1
XM92 net27 clk Vout14 net58 sky130_fd_pr__nfet_01v8 L=0.15 W=1 nf=1 ad='int((1 + 1)/2) * 1 / 1 * 0.29'
+ as='int((1 + 2)/2) * 1 / 1 * 0.29' pd='2*int((1 + 1)/2) * (1 / 1 + 0.29)' ps='2*int((1 + 2)/2) * (1 / 1 + 0.29)'
+ nrd='0.29 / 1 ' nrs='0.29 / 1 ' sa=0 sb=0 sd=0 mult=1 m=1
XM93 net29 clk' Vout15 net59 sky130_fd_pr__pfet_01v8_lvt L=0.35 W=1 nf=1 ad='int((1 + 1)/2) * 1 / 1 *
+ 0.29' as='int((1 + 2)/2) * 1 / 1 * 0.29' pd='2*int((1 + 1)/2) * (1 / 1 + 0.29)' ps='2*int((1 + 2)/2)
+ * (1 / 1 + 0.29)' nrd='0.29 / 1 ' nrs='0.29 / 1 ' sa=0 sb=0 sd=0 mult=1 m=1
XM94 net29 clk Vout15 net60 sky130_fd_pr__nfet_01v8 L=0.15 W=1 nf=1 ad='int((1 + 1)/2) * 1 / 1 * 0.29' as='int((1
+ + 2)/2) * 1 / 1 * 0.29' pd='2*int((1 + 1)/2) * (1 / 1 + 0.29)' ps='2*int((1 + 2)/2) * (1 / 1 + 0.29)' nrd='0.29
+ / 1 ' nrs='0.29 / 1 ' sa=0 sb=0 sd=0 mult=1 m=1
V3 clk gnd pulse(0 1.8 0 100p 100p 4.9n 10n)
V4 clk' gnd PULSE(1.8 0 0 100p 100p 4.9n 10n)
**** begin user architecture code


.lib /home/vboxuser/pdk/sky130A/libs.tech/ngspice/sky130.lib.spice tt

Bcnt cnt 0 V =
+ floor(((1.8-v(vout1))+(1.8-v(vout2))+(1.8-v(vout3))+(1.8-v(vout4))+(1.8-v(vout5))+(1.8-v(vout6))+(1.8-v(vout7))+(1.8-v(vout8))+(1.8-v(vout9))+(1.8-v(vout10))+(1.8-v(vout11))+(1.8-v(vout12))+(1.8-v(vout13))+(1.8-v(vout14))+(1.8-v(vout15)))/1.8+0.5)
Bb3 b3 0 V = floor(v(cnt)/8+0.01)*1.8
Bb2 b2 0 V = (floor(v(cnt)/4+0.01)-2*floor(v(cnt)/8+0.01))*1.8
Bb1 b1 0 V = (floor(v(cnt)/2+0.01)-2*floor(v(cnt)/4+0.01))*1.8
Bb0 b0 0 V = (floor(v(cnt)+0.01)-2*floor(v(cnt)/2+0.01))*1.8

.control
save all
tran 50p 50n
plot v(Vin)
plot v(clk) v(clk')+2.2
plot v(b0) v(b1)+2 v(b2)+4 v(b3)+6
.endc


**** end user architecture code
**.ends
.GLOBAL gnd
.end
